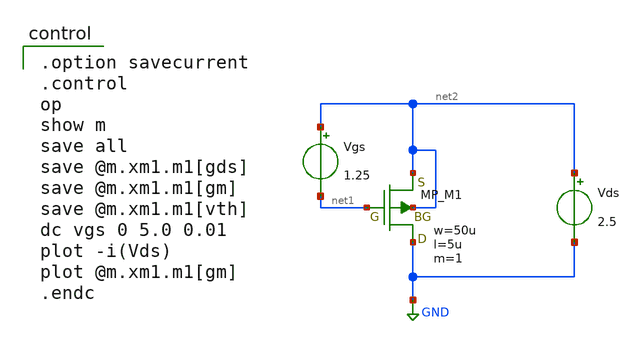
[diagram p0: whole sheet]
** sch_path: member_project/opamp/cat_nekonekone/meas_gm-rds-vth/pmos_idvgs.sch
**.subckt pmos_idvgs
Vgs net2 net1 1.25
Vds net2 GND 2.5
XM1 GND net1 net2 net2 PMOS w=50u l=5u as=0 ad=0 ps=0 pd=0 nrd=0 nrs=0 m=1
**** begin user architecture code

.option savecurrent
.control
op
show m
save all
save @m.xm1.m1[gds]
save @m.xm1.m1[gm]
save @m.xm1.m1[vth]
dc vgs 0 5.0 0.01
plot -i(Vds)
plot @m.xm1.m1[gm]
.endc

 .include $::LIB/ip62_models
**** end user architecture code
**.ends
.GLOBAL GND
.end
